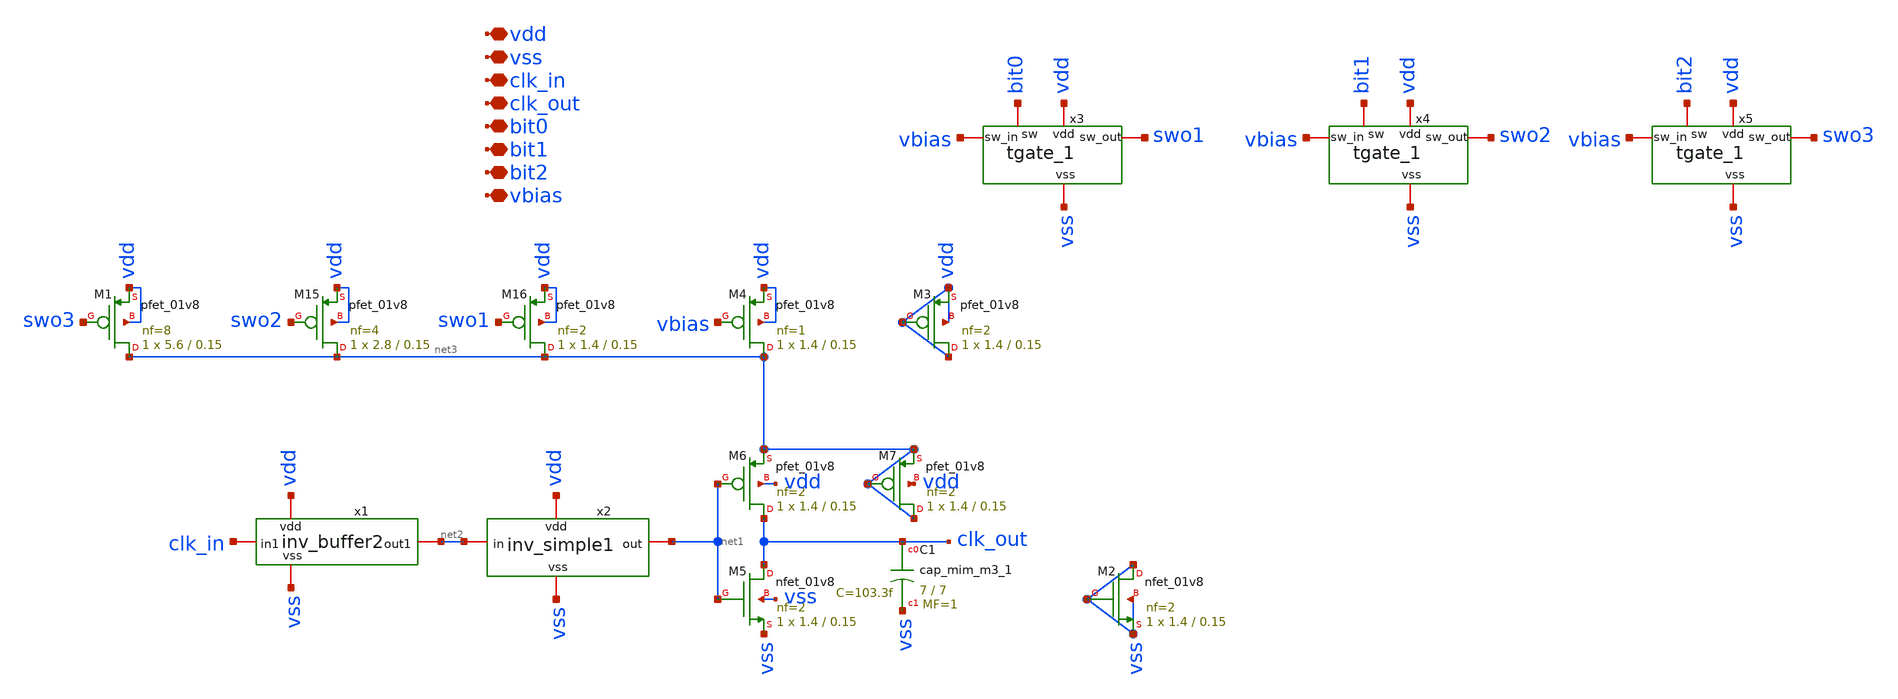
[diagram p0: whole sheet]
** sch_path: xschem/slopebuf.sch
**.subckt slopebuf vdd vss clk_in clk_out bit0 bit1 bit2 vbias
*.iopin vdd
*.iopin vss
*.iopin clk_in
*.iopin clk_out
*.iopin bit0
*.iopin bit1
*.iopin bit2
*.iopin vbias
XM5 clk_out net1 vss vss sky130_fd_pr__nfet_01v8 L=0.15 W=1.4 nf=2 ad='int((nf+1)/2) * W/nf * 0.29' as='int((nf+2)/2) * W/nf * 0.29'
+ pd='2*int((nf+1)/2) * (W/nf + 0.29)' ps='2*int((nf+2)/2) * (W/nf + 0.29)' nrd='0.29 / W' nrs='0.29 / W'
+ sa=0 sb=0 sd=0 mult=1 m=1
XM6 clk_out net1 net3 vdd sky130_fd_pr__pfet_01v8 L=0.15 W=1.4 nf=2 ad='int((nf+1)/2) * W/nf * 0.29'
+ as='int((nf+2)/2) * W/nf * 0.29' pd='2*int((nf+1)/2) * (W/nf + 0.29)' ps='2*int((nf+2)/2) * (W/nf + 0.29)'
+ nrd='0.29 / W' nrs='0.29 / W' sa=0 sb=0 sd=0 mult=1 m=1
XM4 net3 vbias vdd vdd sky130_fd_pr__pfet_01v8 L=0.15 W=1.4 nf=1 ad='int((nf+1)/2) * W/nf * 0.29' as='int((nf+2)/2) * W/nf * 0.29'
+ pd='2*int((nf+1)/2) * (W/nf + 0.29)' ps='2*int((nf+2)/2) * (W/nf + 0.29)' nrd='0.29 / W' nrs='0.29 / W'
+ sa=0 sb=0 sd=0 mult=1 m=1
XM1 net3 swo3 vdd vdd sky130_fd_pr__pfet_01v8 L=0.15 W=5.6 nf=8 ad='int((nf+1)/2) * W/nf * 0.29' as='int((nf+2)/2) * W/nf * 0.29'
+ pd='2*int((nf+1)/2) * (W/nf + 0.29)' ps='2*int((nf+2)/2) * (W/nf + 0.29)' nrd='0.29 / W' nrs='0.29 / W'
+ sa=0 sb=0 sd=0 mult=1 m=1
XM15 net3 swo2 vdd vdd sky130_fd_pr__pfet_01v8 L=0.15 W=2.8 nf=4 ad='int((nf+1)/2) * W/nf * 0.29' as='int((nf+2)/2) * W/nf * 0.29'
+ pd='2*int((nf+1)/2) * (W/nf + 0.29)' ps='2*int((nf+2)/2) * (W/nf + 0.29)' nrd='0.29 / W' nrs='0.29 / W'
+ sa=0 sb=0 sd=0 mult=1 m=1
XM16 net3 swo1 vdd vdd sky130_fd_pr__pfet_01v8 L=0.15 W=1.4 nf=2 ad='int((nf+1)/2) * W/nf * 0.29' as='int((nf+2)/2) * W/nf * 0.29'
+ pd='2*int((nf+1)/2) * (W/nf + 0.29)' ps='2*int((nf+2)/2) * (W/nf + 0.29)' nrd='0.29 / W' nrs='0.29 / W'
+ sa=0 sb=0 sd=0 mult=1 m=1
x1 vdd vss net2 clk_in inv_buffer2
x2 vdd net2 net1 vss inv_simple1
x3 swo1 vbias vss vdd bit0 tgate_1
x4 swo2 vbias vss vdd bit1 tgate_1
x5 swo3 vbias vss vdd bit2 tgate_1
XC1 clk_out vss sky130_fd_pr__cap_mim_m3_1 W=7 L=7 MF=1 m=1
XM2 vss vss vss vss sky130_fd_pr__nfet_01v8 L=0.15 W=1.4 nf=2 ad='int((nf+1)/2) * W/nf * 0.29' as='int((nf+2)/2) * W/nf * 0.29'
+ pd='2*int((nf+1)/2) * (W/nf + 0.29)' ps='2*int((nf+2)/2) * (W/nf + 0.29)' nrd='0.29 / W' nrs='0.29 / W'
+ sa=0 sb=0 sd=0 mult=1 m=1
XM3 vdd vdd vdd vdd sky130_fd_pr__pfet_01v8 L=0.15 W=1.4 nf=2 ad='int((nf+1)/2) * W/nf * 0.29' as='int((nf+2)/2) * W/nf * 0.29'
+ pd='2*int((nf+1)/2) * (W/nf + 0.29)' ps='2*int((nf+2)/2) * (W/nf + 0.29)' nrd='0.29 / W' nrs='0.29 / W'
+ sa=0 sb=0 sd=0 mult=1 m=1
XM7 net3 net3 net3 vdd sky130_fd_pr__pfet_01v8 L=0.15 W=1.4 nf=2 ad='int((nf+1)/2) * W/nf * 0.29' as='int((nf+2)/2) * W/nf * 0.29'
+ pd='2*int((nf+1)/2) * (W/nf + 0.29)' ps='2*int((nf+2)/2) * (W/nf + 0.29)' nrd='0.29 / W' nrs='0.29 / W'
+ sa=0 sb=0 sd=0 mult=1 m=1
**.ends

* expanding   symbol:  inv_buffer2.sym # of pins=4
** sym_path: xschem/inv_buffer2.sym
** sch_path: xschem/inv_buffer2.sch
.subckt inv_buffer2 vdd vss out1 in1
*.iopin in1
*.iopin out1
*.iopin vdd
*.iopin vss
XM4 out1 net1 vss vss sky130_fd_pr__nfet_01v8 L=0.15 W=2.8 nf=4 ad='int((nf+1)/2) * W/nf * 0.29' as='int((nf+2)/2) * W/nf * 0.29'
+ pd='2*int((nf+1)/2) * (W/nf + 0.29)' ps='2*int((nf+2)/2) * (W/nf + 0.29)' nrd='0.29 / W' nrs='0.29 / W'
+ sa=0 sb=0 sd=0 mult=1 m=1
XM1 out1 net1 vdd vdd sky130_fd_pr__pfet_01v8 L=0.15 W=5.6 nf=8 ad='int((nf+1)/2) * W/nf * 0.29' as='int((nf+2)/2) * W/nf * 0.29'
+ pd='2*int((nf+1)/2) * (W/nf + 0.29)' ps='2*int((nf+2)/2) * (W/nf + 0.29)' nrd='0.29 / W' nrs='0.29 / W'
+ sa=0 sb=0 sd=0 mult=1 m=1
XM5 vdd vdd vdd vdd sky130_fd_pr__pfet_01v8 L=0.15 W=1.4 nf=2 ad='int((nf+1)/2) * W/nf * 0.29' as='int((nf+2)/2) * W/nf * 0.29'
+ pd='2*int((nf+1)/2) * (W/nf + 0.29)' ps='2*int((nf+2)/2) * (W/nf + 0.29)' nrd='0.29 / W' nrs='0.29 / W'
+ sa=0 sb=0 sd=0 mult=1 m=1
XM6 vss vss vss vss sky130_fd_pr__nfet_01v8 L=0.15 W=1.4 nf=2 ad='int((nf+1)/2) * W/nf * 0.29' as='int((nf+2)/2) * W/nf * 0.29'
+ pd='2*int((nf+1)/2) * (W/nf + 0.29)' ps='2*int((nf+2)/2) * (W/nf + 0.29)' nrd='0.29 / W' nrs='0.29 / W'
+ sa=0 sb=0 sd=0 mult=1 m=1
x1 vdd in1 net1 vss inv_simple1
.ends


* expanding   symbol:  inv_simple1.sym # of pins=4
** sym_path: xschem/inv_simple1.sym
** sch_path: xschem/inv_simple1.sch
.subckt inv_simple1 vdd in out vss
*.iopin in
*.iopin vdd
*.iopin vss
*.iopin out
XM19 out in vss vss sky130_fd_pr__nfet_01v8 L=0.15 W=1.4 nf=1 ad='int((nf+1)/2) * W/nf * 0.29' as='int((nf+2)/2) * W/nf * 0.29'
+ pd='2*int((nf+1)/2) * (W/nf + 0.29)' ps='2*int((nf+2)/2) * (W/nf + 0.29)' nrd='0.29 / W' nrs='0.29 / W'
+ sa=0 sb=0 sd=0 mult=1 m=1
XM20 out in vdd vdd sky130_fd_pr__pfet_01v8 L=0.15 W=2.8 nf=1 ad='int((nf+1)/2) * W/nf * 0.29' as='int((nf+2)/2) * W/nf * 0.29'
+ pd='2*int((nf+1)/2) * (W/nf + 0.29)' ps='2*int((nf+2)/2) * (W/nf + 0.29)' nrd='0.29 / W' nrs='0.29 / W'
+ sa=0 sb=0 sd=0 mult=1 m=1
XM1 vdd vdd vdd vdd sky130_fd_pr__pfet_01v8 L=0.15 W=1.4 nf=1 ad='int((nf+1)/2) * W/nf * 0.29' as='int((nf+2)/2) * W/nf * 0.29'
+ pd='2*int((nf+1)/2) * (W/nf + 0.29)' ps='2*int((nf+2)/2) * (W/nf + 0.29)' nrd='0.29 / W' nrs='0.29 / W'
+ sa=0 sb=0 sd=0 mult=1 m=1
XM2 vss vss vss vss sky130_fd_pr__nfet_01v8 L=0.15 W=1.4 nf=1 ad='int((nf+1)/2) * W/nf * 0.29' as='int((nf+2)/2) * W/nf * 0.29'
+ pd='2*int((nf+1)/2) * (W/nf + 0.29)' ps='2*int((nf+2)/2) * (W/nf + 0.29)' nrd='0.29 / W' nrs='0.29 / W'
+ sa=0 sb=0 sd=0 mult=1 m=1
.ends


* expanding   symbol:  tgate_1.sym # of pins=5
** sym_path: xschem/tgate_1.sym
** sch_path: xschem/tgate_1.sch
.subckt tgate_1 sw_out sw_in vss vdd sw
*.iopin sw_in
*.iopin vdd
*.iopin vss
*.iopin sw
*.iopin sw_out
XM17 sw_out sw sw_in vdd sky130_fd_pr__pfet_01v8 L=0.15 W=1.4 nf=2 ad='int((nf+1)/2) * W/nf * 0.29' as='int((nf+2)/2) * W/nf * 0.29'
+ pd='2*int((nf+1)/2) * (W/nf + 0.29)' ps='2*int((nf+2)/2) * (W/nf + 0.29)' nrd='0.29 / W' nrs='0.29 / W'
+ sa=0 sb=0 sd=0 mult=1 m=1
XM18 sw_in net1 sw_out vss sky130_fd_pr__nfet_01v8 L=0.15 W=1.4 nf=2 ad='int((nf+1)/2) * W/nf * 0.29'
+ as='int((nf+2)/2) * W/nf * 0.29' pd='2*int((nf+1)/2) * (W/nf + 0.29)' ps='2*int((nf+2)/2) * (W/nf + 0.29)'
+ nrd='0.29 / W' nrs='0.29 / W' sa=0 sb=0 sd=0 mult=1 m=1
x1 vdd sw net1 vss inv_simple1
XM1 sw_out sw_out sw_out vdd sky130_fd_pr__pfet_01v8 L=0.15 W=1.4 nf=2 ad='int((nf+1)/2) * W/nf * 0.29'
+ as='int((nf+2)/2) * W/nf * 0.29' pd='2*int((nf+1)/2) * (W/nf + 0.29)' ps='2*int((nf+2)/2) * (W/nf + 0.29)'
+ nrd='0.29 / W' nrs='0.29 / W' sa=0 sb=0 sd=0 mult=1 m=1
XM2 sw_out sw_out sw_out vss sky130_fd_pr__nfet_01v8 L=0.15 W=1.4 nf=2 ad='int((nf+1)/2) * W/nf * 0.29'
+ as='int((nf+2)/2) * W/nf * 0.29' pd='2*int((nf+1)/2) * (W/nf + 0.29)' ps='2*int((nf+2)/2) * (W/nf + 0.29)'
+ nrd='0.29 / W' nrs='0.29 / W' sa=0 sb=0 sd=0 mult=1 m=1
.ends

.end
